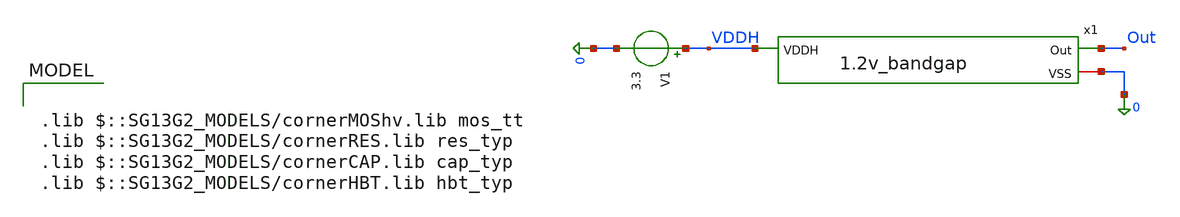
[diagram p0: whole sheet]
** sch_path: sar_adc/xschem/blocks/bandgap/1.2v_bandgap_tb.sch
**.subckt 1.2v_bandgap_tb
V1 VDDH 0 3.3
x1 VDDH Out 0 1.2v_bandgap
**** begin user architecture code

.lib $::SG13G2_MODELS/cornerMOShv.lib mos_tt
.lib $::SG13G2_MODELS/cornerRES.lib res_typ
.lib $::SG13G2_MODELS/cornerCAP.lib cap_typ
.lib $::SG13G2_MODELS/cornerHBT.lib hbt_typ




* Gear integration: suppresses trapezoidal ringing that blocks
* transient-op convergence at cold corner (-40C). Required for full-range sim.
.options method=gear

.ic v(VDDH)=3.3 v(x1.net1)=0 v(x1.v_c1)=0 v(x1.net3)=0

.control

save all
set temp=27

op
echo === OP node voltages (27C) ===
print v(x1.Inp) v(x1.Inn) v(x1.net1) v(x1.net2) v(x1.net_1) v(Out)
* Startup branch currents (Vmeas are inside x1, so use hierarchical name):
print i(v.x1.vmeas1) i(v.x1.vmeas2) i(v.x1.vmeas3)

dc temp -40 125 1

* Correct node map for THIS netlist:
*  Q1 emitter = net1 (8x)      Q2 emitter = Inn (1x)     Q3 emitter = net2
*  PTAT resistor XR1 is between net1 and Inp  ->  dVbe = Inp - net1
*  net3/net4 = startup PMOS sources (~3.3V), NOT diode nodes

let vbe    = x1.Inn                 $ CTAT reference (Q2 Vbe)
let vdvbe  = x1.Inp - x1.net1       $ PTAT voltage across XR1 (13k)
let veq    = out                    $ bandgap output

* Vbe CTAT stats
let vbe_max = vecmax(vbe)
let vbe_min = vecmin(vbe)
let vbe_nom = mean(vbe)
let tc_vbe  = ((vbe_max - vbe_min) / vbe_nom) * 1e6 / 165

* Delta_Vbe PTAT stats
let vr_max = vecmax(vdvbe)
let vr_min = vecmin(vdvbe)
let vr_nom = mean(vdvbe)
let tc_vr  = ((vr_max - vr_min) / vr_nom) * 1e6 / 165

* PTAT current  (XR1 = 100u/2u rppd ~ 13 kOhm)
let i_ptat    = vdvbe / 13e3
let i_ptat_ua = i_ptat * 1e6

* Bandgap output stats
let veq_max = vecmax(veq)
let veq_min = vecmin(veq)
let veq_nom = mean(veq)
let tc_eq   = ((veq_max - veq_min) / veq_nom) * 1e6 / 165

echo === Vbe CTAT (Inn = Q2 emitter) ===
print vbe_max vbe_min vbe_nom tc_vbe

echo === Delta_Vbe PTAT (Inp - net1, across XR1) ===
print vr_max vr_min vr_nom tc_vr

echo === I_PTAT uA ===
print vecmax(i_ptat_ua) vecmin(i_ptat_ua) mean(i_ptat_ua)

echo === Bandgap Output (Out) ===
print veq_max veq_min veq_nom tc_eq

echo === Q3 emitter (net2) ===
print vecmax(x1.net2) vecmin(x1.net2) mean(x1.net2)

let veq_center = (veq_max + veq_min) / 2
let tc_eq_pp = (veq_max - veq_min) / veq_center * 1e6 / 165
echo === TC (peak-to-peak / center) ===
print tc_eq_pp

plot x1.Inn title 'Vbe vs. T (CTAT)'
plot x1.Inp - x1.net1 title 'Delta_Vbe vs. T (PTAT, across XR1)'
plot out title 'Bandgap output vs. T'
plot i_ptat_ua title 'I_PTAT uA vs. T'


* Bandgap startup analysis
tran 50p 300n uic
plot x1.net_1 x1.v_c1 x1.net_3 title 'Startup circuit voltages'
plot out title 'Output voltage at startup'
plot x1.Inp x1.Inn title 'Equilibrium voltages at startup'
plot i(v.x1.Vmeas1) i(v.x1.Vmeas2) i(v.x1.Vmeas3) xlimit 0 20n title 'Startup circuit currents'



.endc


**** end user architecture code
**.ends
.end
